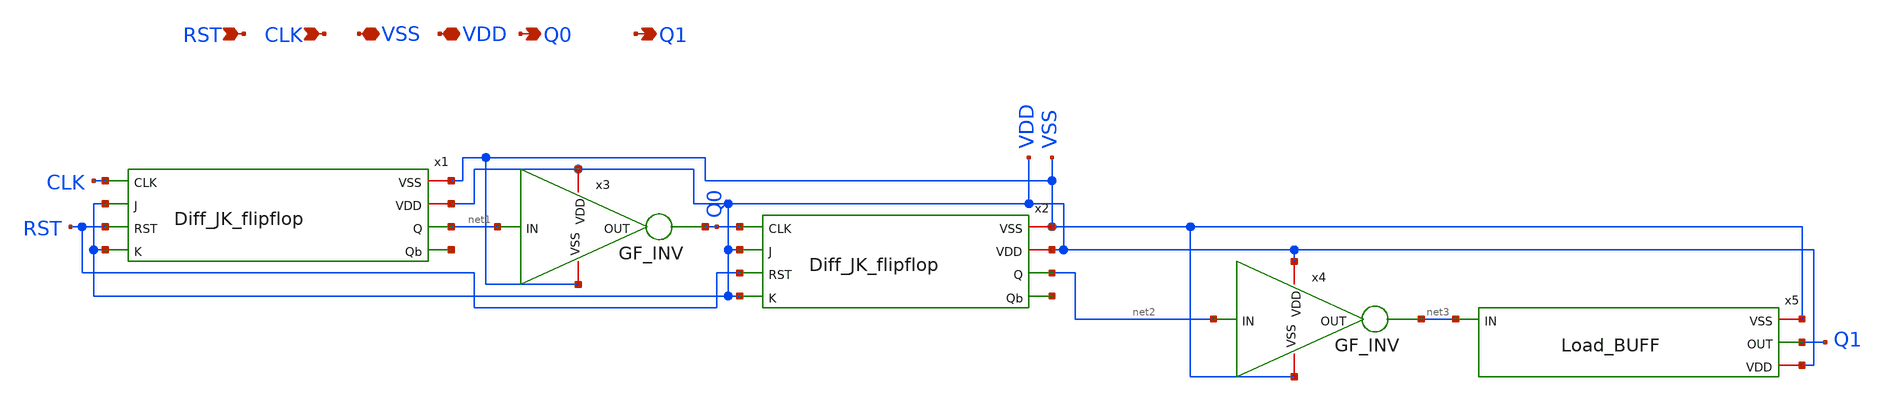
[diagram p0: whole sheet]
** sch_path: Clock_Generator_PAKISTAN_02/Schematics/Diff_CLK_div_4.sch
**.subckt Diff_CLK_div_4 CLK VSS VDD Q0 Q1 RST
*.ipin CLK
*.iopin VSS
*.iopin VDD
*.opin Q0
*.opin Q1
*.ipin RST
x1 CLK VSS VDD net1 VDD net4 RST VDD Diff_JK_flipflop
x2 Q0 VSS VDD net2 VDD net5 RST VDD Diff_JK_flipflop
x3 VSS VDD Q0 net1 GF_INV
x4 VSS VDD net3 net2 GF_INV
x5 VSS net3 Q1 VDD Load_BUFF
**.ends
.end
